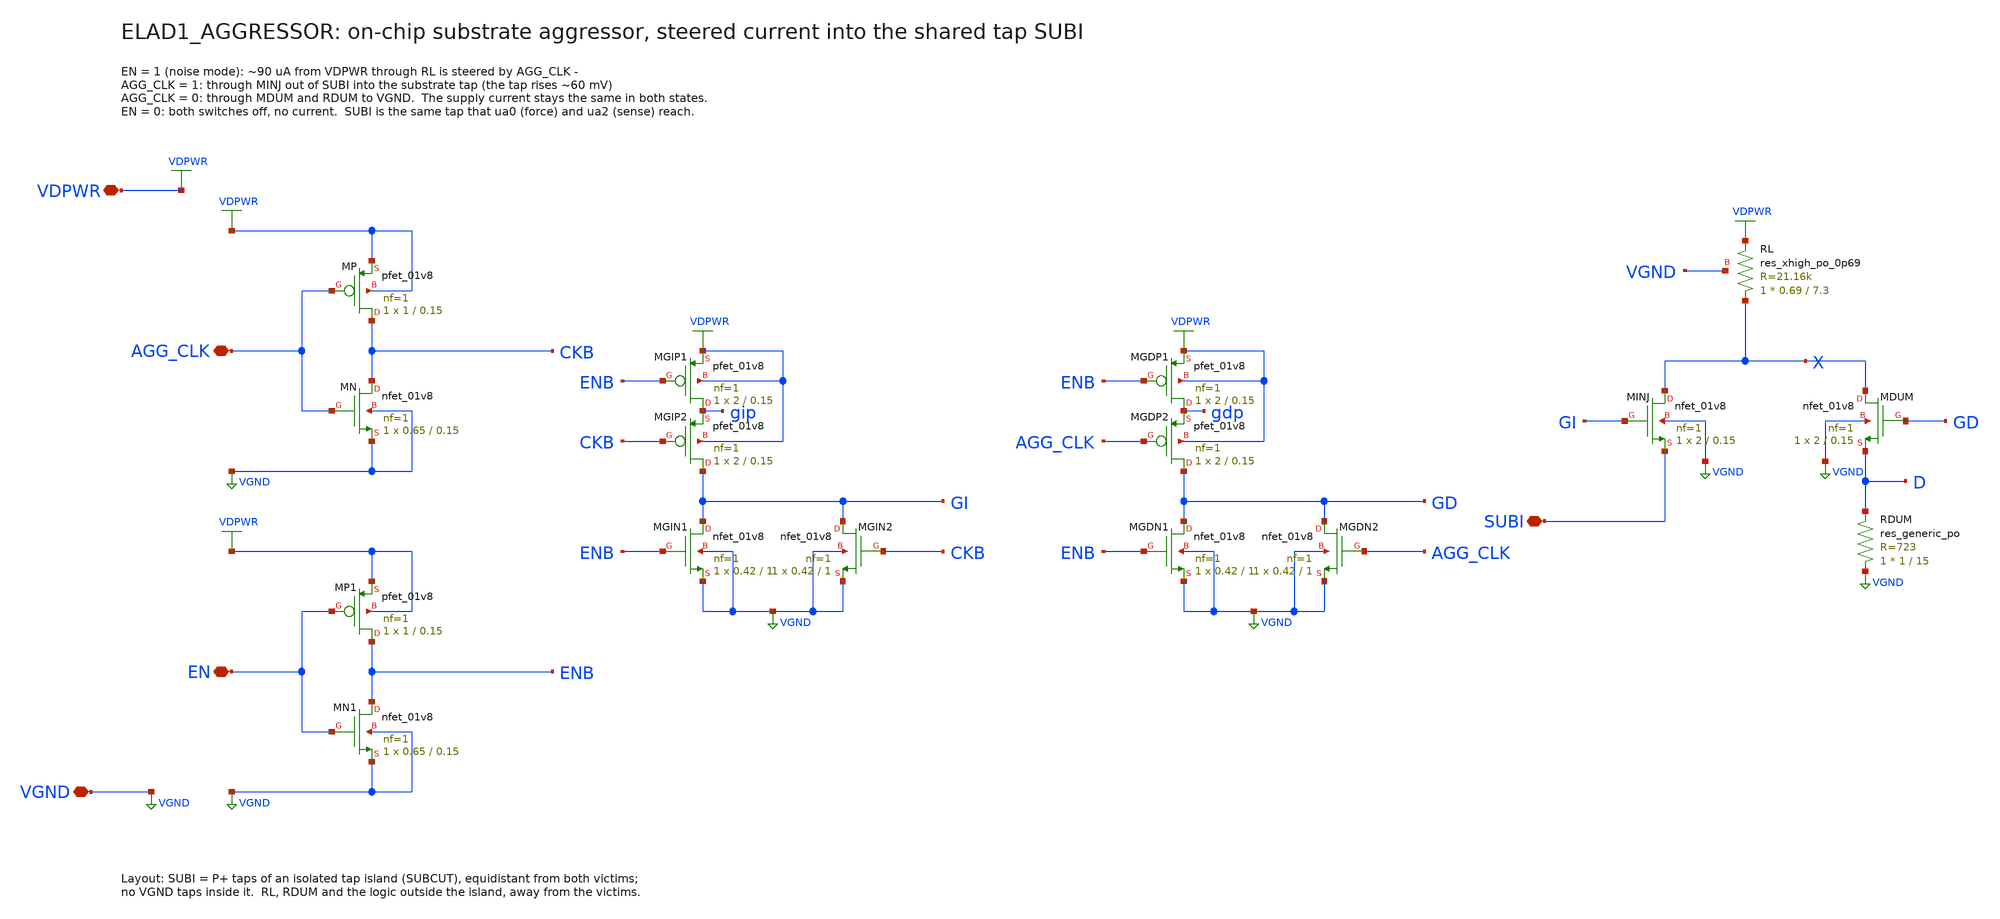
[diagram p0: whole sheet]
** sch_path: cells/ELAD1_AGGRESSOR/schematic/ELAD1_AGGRESSOR.sch
**.subckt ELAD1_AGGRESSOR AGG_CLK EN VDPWR VGND SUBI
*.iopin AGG_CLK
*.iopin EN
*.iopin VDPWR
*.iopin VGND
*.iopin SUBI
XMGIP1 gip ENB VDPWR VDPWR sky130_fd_pr__pfet_01v8 L=0.15 W=2 nf=1 ad='int((nf+1)/2) * W/nf * 0.29' as='int((nf+2)/2) * W/nf * 0.29'
+ pd='2*int((nf+1)/2) * (W/nf + 0.29)' ps='2*int((nf+2)/2) * (W/nf + 0.29)' nrd='0.29 / W' nrs='0.29 / W'
+ sa=0 sb=0 sd=0 mult=1 m=1
XMGIP2 GI CKB gip VDPWR sky130_fd_pr__pfet_01v8 L=0.15 W=2 nf=1 ad='int((nf+1)/2) * W/nf * 0.29' as='int((nf+2)/2) * W/nf * 0.29'
+ pd='2*int((nf+1)/2) * (W/nf + 0.29)' ps='2*int((nf+2)/2) * (W/nf + 0.29)' nrd='0.29 / W' nrs='0.29 / W'
+ sa=0 sb=0 sd=0 mult=1 m=1
XMGIN1 GI ENB VGND VGND sky130_fd_pr__nfet_01v8 L=1 W=0.42 nf=1 ad='int((1 + 1)/2) * 0.42 / 1 * 0.29'
+ as='int((1 + 2)/2) * 0.42 / 1 * 0.29' pd='2*int((1 + 1)/2) * (0.42 / 1 + 0.29)' ps='2*int((1 + 2)/2) * (0.42 / 1 + 0.29)'
+ nrd='0.29 / 0.42 ' nrs='0.29 / 0.42 ' sa=0 sb=0 sd=0 mult=1 m=1
XMGIN2 GI CKB VGND VGND sky130_fd_pr__nfet_01v8 L=1 W=0.42 nf=1 ad='int((1 + 1)/2) * 0.42 / 1 * 0.29'
+ as='int((1 + 2)/2) * 0.42 / 1 * 0.29' pd='2*int((1 + 1)/2) * (0.42 / 1 + 0.29)' ps='2*int((1 + 2)/2) * (0.42 / 1 + 0.29)'
+ nrd='0.29 / 0.42 ' nrs='0.29 / 0.42 ' sa=0 sb=0 sd=0 mult=1 m=1
XMGDP1 gdp ENB VDPWR VDPWR sky130_fd_pr__pfet_01v8 L=0.15 W=2 nf=1 ad='int((nf+1)/2) * W/nf * 0.29' as='int((nf+2)/2) * W/nf * 0.29'
+ pd='2*int((nf+1)/2) * (W/nf + 0.29)' ps='2*int((nf+2)/2) * (W/nf + 0.29)' nrd='0.29 / W' nrs='0.29 / W'
+ sa=0 sb=0 sd=0 mult=1 m=1
XMGDP2 GD AGG_CLK gdp VDPWR sky130_fd_pr__pfet_01v8 L=0.15 W=2 nf=1 ad='int((nf+1)/2) * W/nf * 0.29'
+ as='int((nf+2)/2) * W/nf * 0.29' pd='2*int((nf+1)/2) * (W/nf + 0.29)' ps='2*int((nf+2)/2) * (W/nf + 0.29)'
+ nrd='0.29 / W' nrs='0.29 / W' sa=0 sb=0 sd=0 mult=1 m=1
XMGDN1 GD ENB VGND VGND sky130_fd_pr__nfet_01v8 L=1 W=0.42 nf=1 ad='int((1 + 1)/2) * 0.42 / 1 * 0.29'
+ as='int((1 + 2)/2) * 0.42 / 1 * 0.29' pd='2*int((1 + 1)/2) * (0.42 / 1 + 0.29)' ps='2*int((1 + 2)/2) * (0.42 / 1 + 0.29)'
+ nrd='0.29 / 0.42 ' nrs='0.29 / 0.42 ' sa=0 sb=0 sd=0 mult=1 m=1
XMGDN2 GD AGG_CLK VGND VGND sky130_fd_pr__nfet_01v8 L=1 W=0.42 nf=1 ad='int((1 + 1)/2) * 0.42 / 1 * 0.29'
+ as='int((1 + 2)/2) * 0.42 / 1 * 0.29' pd='2*int((1 + 1)/2) * (0.42 / 1 + 0.29)' ps='2*int((1 + 2)/2) * (0.42 / 1 + 0.29)'
+ nrd='0.29 / 0.42 ' nrs='0.29 / 0.42 ' sa=0 sb=0 sd=0 mult=1 m=1
XRL X VDPWR VGND sky130_fd_pr__res_xhigh_po_0p69 L=7.3 mult=1 m=1
XMINJ X GI SUBI VGND sky130_fd_pr__nfet_01v8 L=0.15 W=2 nf=1 ad='int((1 + 1)/2) * 2 / 1 * 0.29' as='int((1 + 2)/2) * 2 / 1 * 0.29'
+ pd='2*int((1 + 1)/2) * (2 / 1 + 0.29)' ps='2*int((1 + 2)/2) * (2 / 1 + 0.29)' nrd='0.29 / 2 ' nrs='0.29 / 2 '
+ sa=0 sb=0 sd=0 mult=1 m=1
XMDUM X GD D VGND sky130_fd_pr__nfet_01v8 L=0.15 W=2 nf=1 ad='int((1 + 1)/2) * 2 / 1 * 0.29' as='int((1 + 2)/2) * 2 / 1 * 0.29'
+ pd='2*int((1 + 1)/2) * (2 / 1 + 0.29)' ps='2*int((1 + 2)/2) * (2 / 1 + 0.29)' nrd='0.29 / 2 ' nrs='0.29 / 2 '
+ sa=0 sb=0 sd=0 mult=1 m=1
XRDUM VGND D sky130_fd_pr__res_generic_po W=1 L=15 m=1
XMP CKB AGG_CLK VDPWR VDPWR sky130_fd_pr__pfet_01v8 L=0.15 W=1 nf=1 ad='int((nf+1)/2) * W/nf * 0.29'
+ as='int((nf+2)/2) * W/nf * 0.29' pd='2*int((nf+1)/2) * (W/nf + 0.29)' ps='2*int((nf+2)/2) * (W/nf + 0.29)'
+ nrd='0.29 / W' nrs='0.29 / W' sa=0 sb=0 sd=0 mult=1 m=1
XMN CKB AGG_CLK VGND VGND sky130_fd_pr__nfet_01v8 L=0.15 W=0.65 nf=1 ad='int((1 + 1)/2) * 0.65 / 1 * 0.29'
+ as='int((1 + 2)/2) * 0.65 / 1 * 0.29' pd='2*int((1 + 1)/2) * (0.65 / 1 + 0.29)' ps='2*int((1 + 2)/2) * (0.65 / 1 + 0.29)'
+ nrd='0.29 / 0.65 ' nrs='0.29 / 0.65 ' sa=0 sb=0 sd=0 mult=1 m=1
XMP1 ENB EN VDPWR VDPWR sky130_fd_pr__pfet_01v8 L=0.15 W=1 nf=1 ad='int((nf+1)/2) * W/nf * 0.29' as='int((nf+2)/2) * W/nf * 0.29'
+ pd='2*int((nf+1)/2) * (W/nf + 0.29)' ps='2*int((nf+2)/2) * (W/nf + 0.29)' nrd='0.29 / W' nrs='0.29 / W'
+ sa=0 sb=0 sd=0 mult=1 m=1
XMN1 ENB EN VGND VGND sky130_fd_pr__nfet_01v8 L=0.15 W=0.65 nf=1 ad='int((1 + 1)/2) * 0.65 / 1 * 0.29'
+ as='int((1 + 2)/2) * 0.65 / 1 * 0.29' pd='2*int((1 + 1)/2) * (0.65 / 1 + 0.29)' ps='2*int((1 + 2)/2) * (0.65 / 1 + 0.29)'
+ nrd='0.29 / 0.65 ' nrs='0.29 / 0.65 ' sa=0 sb=0 sd=0 mult=1 m=1
**.ends
.end
